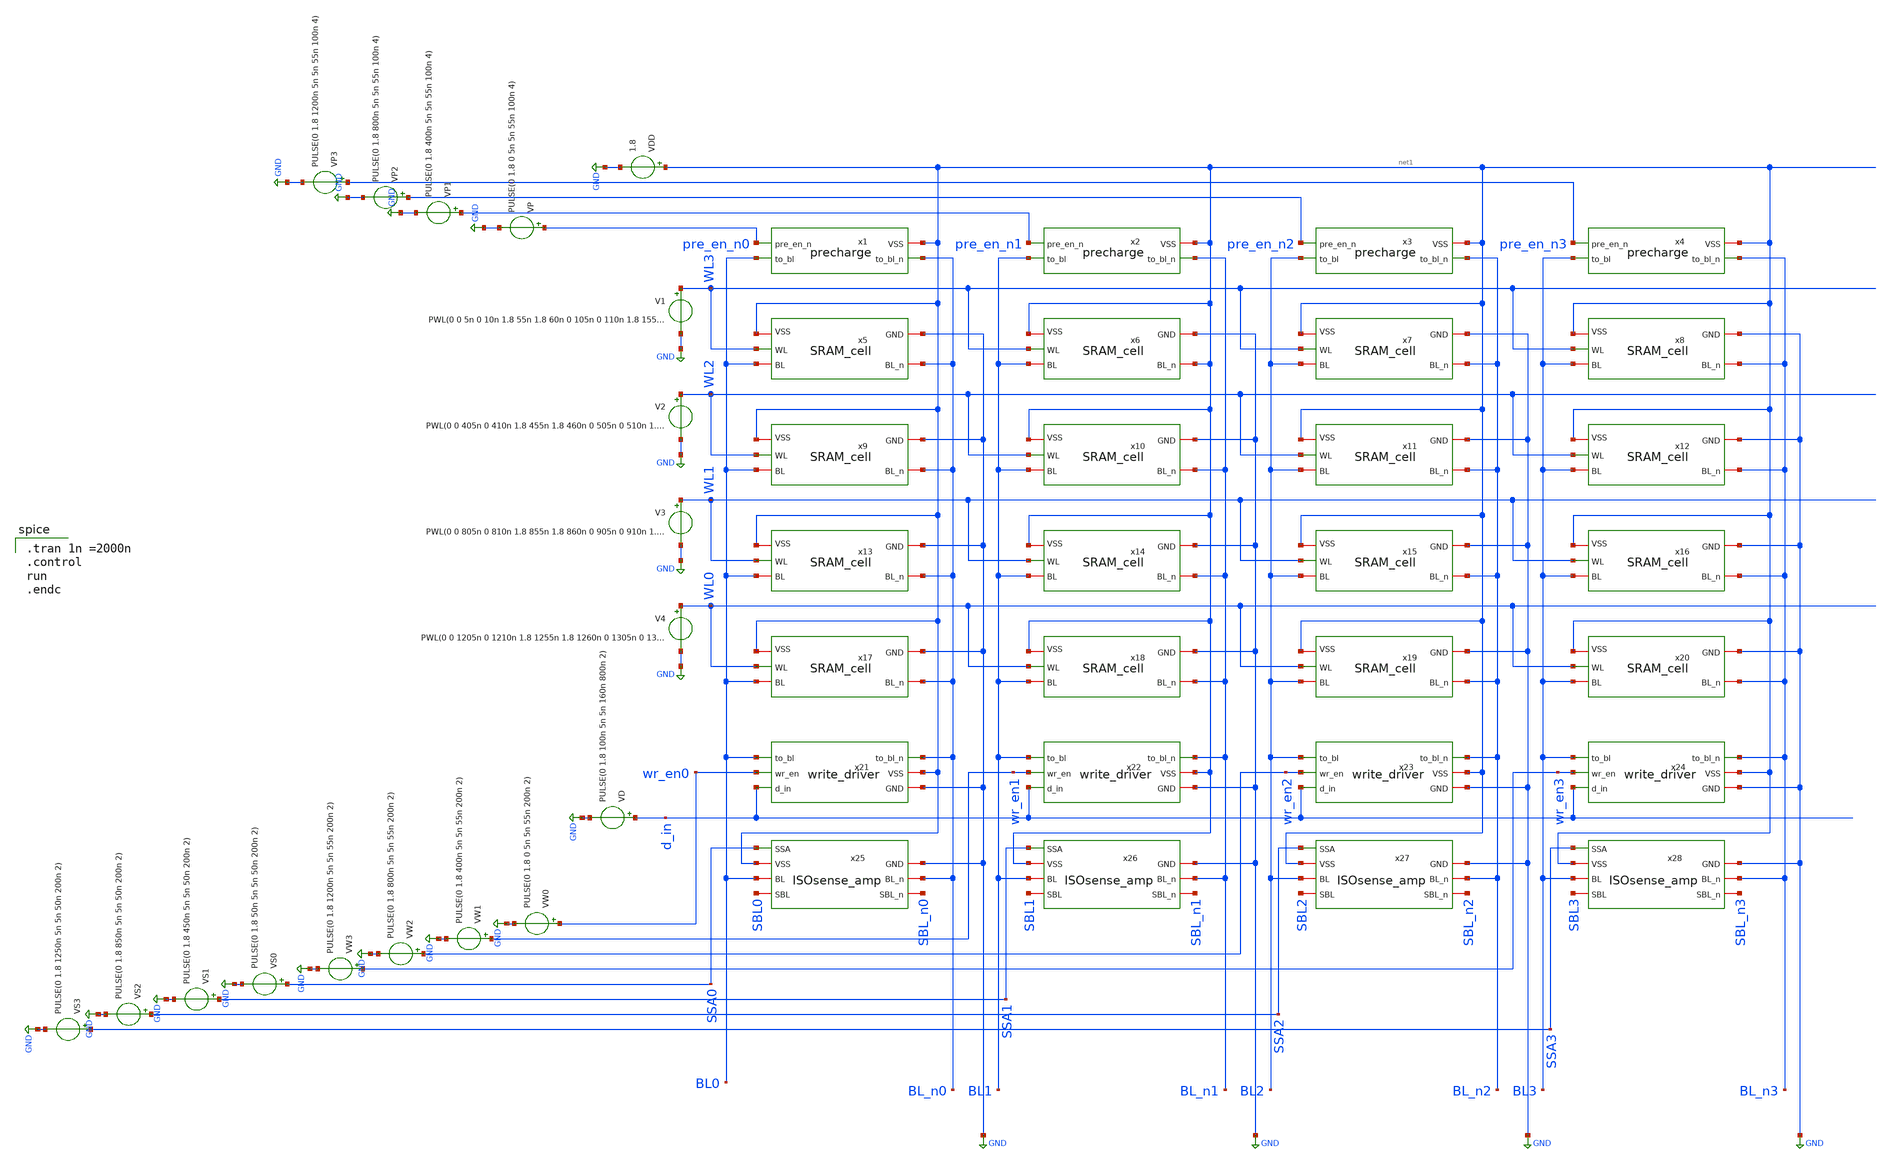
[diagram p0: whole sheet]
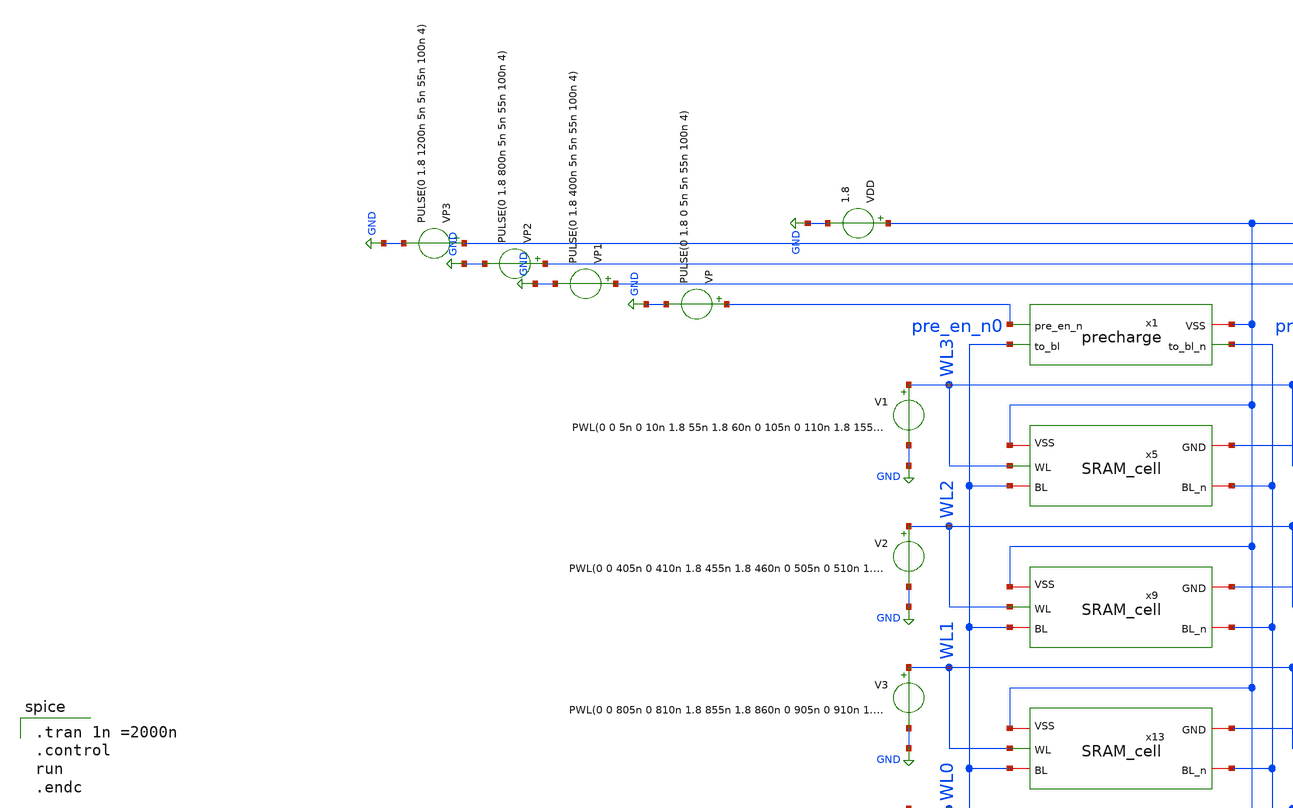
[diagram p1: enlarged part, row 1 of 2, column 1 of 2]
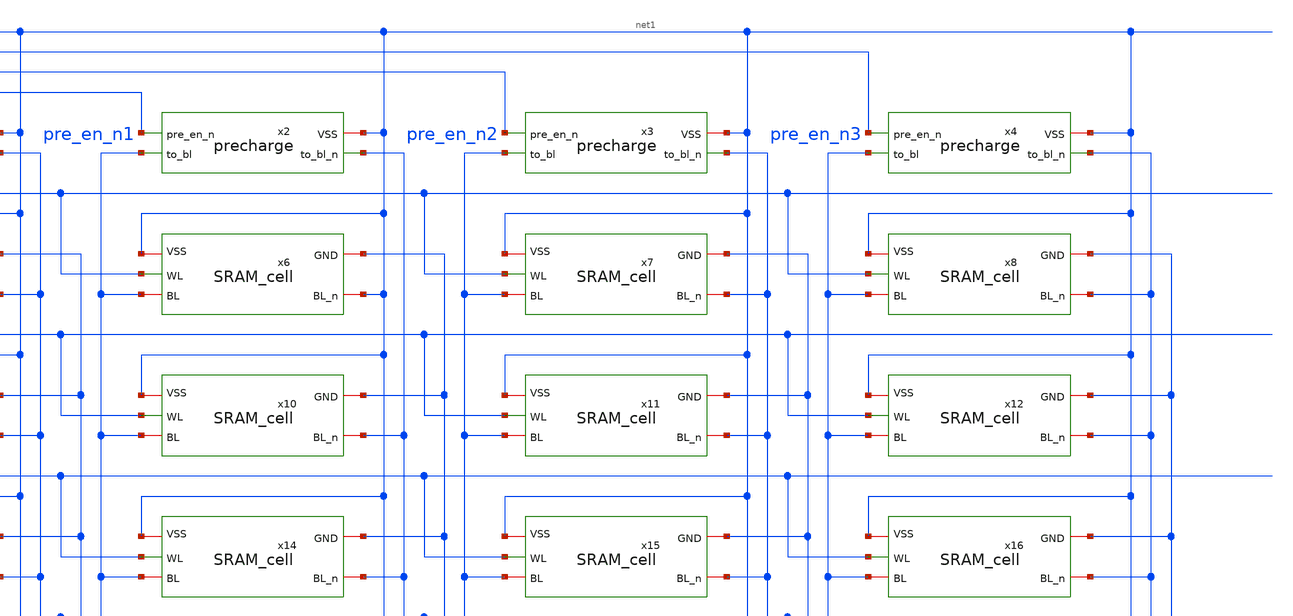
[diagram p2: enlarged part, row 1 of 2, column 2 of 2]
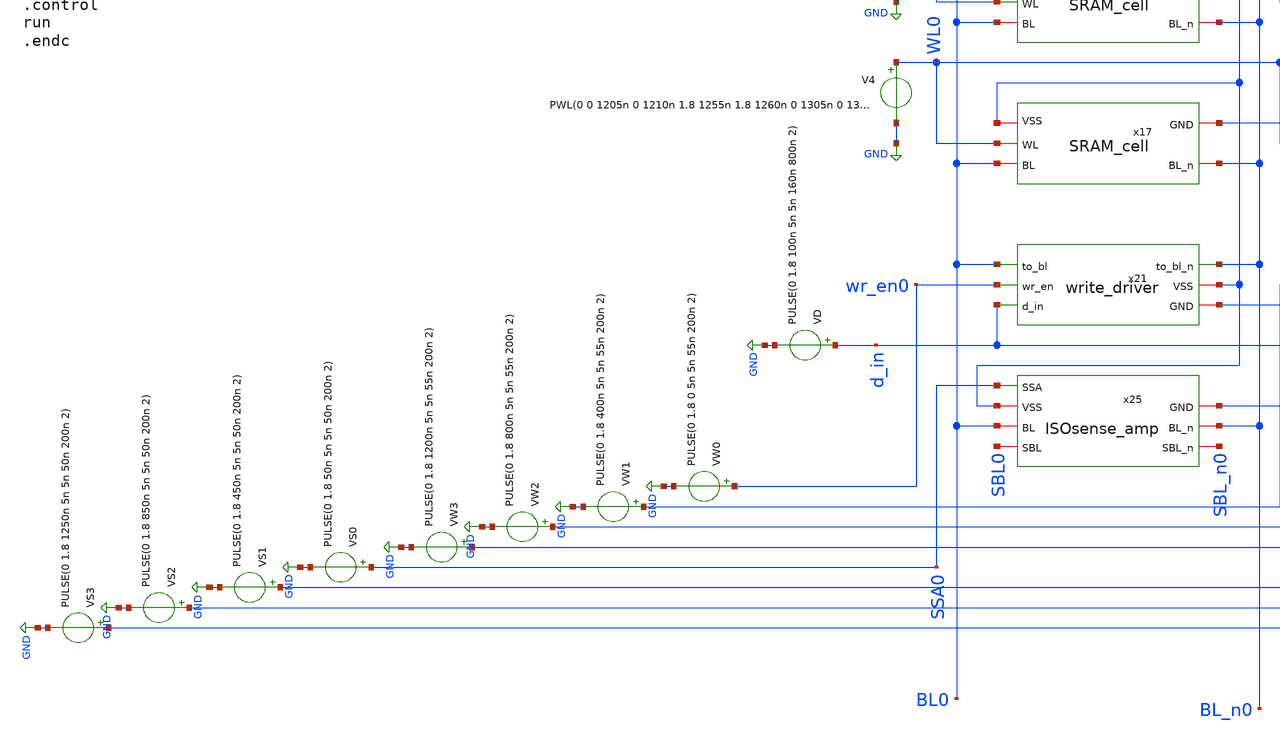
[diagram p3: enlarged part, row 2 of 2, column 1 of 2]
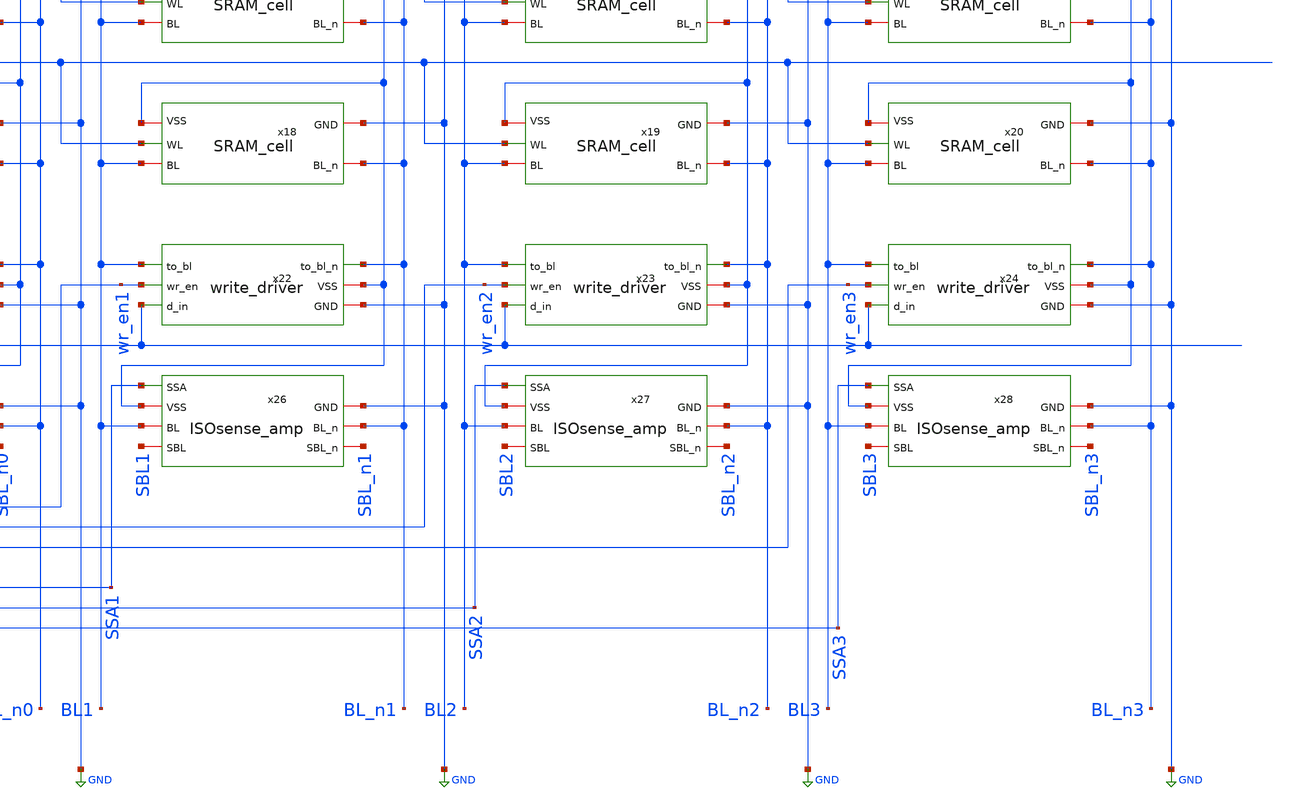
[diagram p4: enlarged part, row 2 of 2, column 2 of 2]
** sch_path: 4x4_SRAM.sch
**.subckt 4x4_SRAM
x1 net1 BL_n0 BL0 pre_en_n0 precharge
x5 WL3 net1 BL_n0 BL0 GND SRAM_cell
x9 WL2 net1 BL_n0 BL0 GND SRAM_cell
x13 WL1 net1 BL_n0 BL0 GND SRAM_cell
x17 WL0 net1 BL_n0 BL0 GND SRAM_cell
x21 BL_n0 BL0 wr_en0 net1 d_in GND write_driver
x25 SSA0 BL0 BL_n0 net1 SBL0 SBL_n0 GND ISOsense_amp
VDD net1 GND 1.8
VP pre_en_n0 GND PULSE(0 1.8 0 5n 5n 55n 100n 4)
V1 WL3 GND PWL(0 0 5n 0 10n 1.8 55n 1.8 60n 0 105n 0 110n 1.8 155n 1.8 160n 0 205n 0 210n 1.8 255n
+ 1.8 260n 0 305n 0 310n 1.8 355n 1.8 360n 0 1600n 0)
VW0 wr_en0 GND PULSE(0 1.8 0 5n 5n 55n 200n 2)
VD d_in GND PULSE(0 1.8 100n 5n 5n 160n 800n 2)
VS0 SSA0 GND PULSE(0 1.8 50n 5n 5n 50n 200n 2)
V2 WL2 GND PWL(0 0 405n 0 410n 1.8 455n 1.8 460n 0 505n 0 510n 1.8 555n 1.8 560n 0 605n 0 610n 1.8
+ 655n 1.8 660n 0 705n 0 710n 1.8 755n 1.8 760n 0 1600n 0)
V3 WL1 GND PWL(0 0 805n 0 810n 1.8 855n 1.8 860n 0 905n 0 910n 1.8 955n 1.8 960n 0 1005n 0 1010n 1.8
+ 1055n 1.8 1060n 0 1105n 0 1110n 1.8 1155n 1.8 1160n 0 1600n 0)
V4 WL0 GND PWL(0 0 1205n 0 1210n 1.8 1255n 1.8 1260n 0 1305n 0 1310n 1.8 1355n 1.8 1360n 0 1405n 0
+ 1410n 1.8 1455n 1.8 1460n 0 1505n 0 1510n 1.8 1555n 1.8 1560n 0 1600n 0
x2 net1 BL_n1 BL1 pre_en_n1 precharge
x3 net1 BL_n2 BL2 pre_en_n2 precharge
x4 net1 BL_n3 BL3 pre_en_n3 precharge
x6 WL3 net1 net1 BL1 GND SRAM_cell
x7 WL3 net1 BL_n2 BL2 GND SRAM_cell
x8 WL3 net1 BL_n3 BL3 GND SRAM_cell
x10 WL2 net1 BL_n1 BL1 GND SRAM_cell
x11 WL2 net1 BL_n2 BL2 GND SRAM_cell
x12 WL2 net1 BL_n3 BL3 GND SRAM_cell
x14 WL1 net1 BL_n1 BL1 GND SRAM_cell
x15 WL1 net1 BL_n2 BL2 GND SRAM_cell
x16 WL1 net1 BL_n3 BL3 GND SRAM_cell
x18 WL0 net1 BL_n1 BL1 GND SRAM_cell
x19 WL0 net1 BL_n2 BL2 GND SRAM_cell
x20 WL0 net1 BL_n3 BL3 GND SRAM_cell
x22 BL_n1 BL1 wr_en1 net1 d_in GND write_driver
x23 BL_n2 BL2 wr_en2 net1 d_in GND write_driver
x24 BL_n3 BL3 wr_en3 net1 d_in GND write_driver
x26 SSA1 BL1 BL_n1 net1 SBL1 SBL_n1 GND ISOsense_amp
x27 SSA2 BL2 BL_n2 net1 SBL2 SBL_n2 GND ISOsense_amp
x28 SSA3 BL3 BL_n3 net1 SBL3 SBL_n3 GND ISOsense_amp
VW1 wr_en1 GND PULSE(0 1.8 400n 5n 5n 55n 200n 2)
VW2 wr_en2 GND PULSE(0 1.8 800n 5n 5n 55n 200n 2)
VW3 wr_en3 GND PULSE(0 1.8 1200n 5n 5n 55n 200n 2)
VS1 SSA1 GND PULSE(0 1.8 450n 5n 5n 50n 200n 2)
VS2 SSA2 GND PULSE(0 1.8 850n 5n 5n 50n 200n 2)
VS3 SSA3 GND PULSE(0 1.8 1250n 5n 5n 50n 200n 2)
VP1 pre_en_n1 GND PULSE(0 1.8 400n 5n 5n 55n 100n 4)
VP2 pre_en_n2 GND PULSE(0 1.8 800n 5n 5n 55n 100n 4)
VP3 pre_en_n3 GND PULSE(0 1.8 1200n 5n 5n 55n 100n 4)
**** begin user architecture code
 .lib $::SKYWATER_MODELS/sky130.lib.spice tt

.tran 1n =2000n
.control
run
.endc

**** end user architecture code
**.ends

* expanding   symbol:  EE431_FINALPROJECT/proj_SRAM/precharge.sym # of pins=4
** sym_path: precharge.sym
** sch_path: precharge.sch
.subckt precharge VSS to_bl_n to_bl pre_en_n
*.ipin pre_en_n
*.opin to_bl
*.opin to_bl_n
*.iopin VSS
XM1 to_bl_n pre_en_n VSS VSS sky130_fd_pr__pfet_01v8 L=0.25 W=0.5 nf=1 ad='int((nf+1)/2) * W/nf * 0.29'
+ as='int((nf+2)/2) * W/nf * 0.29' pd='2*int((nf+1)/2) * (W/nf + 0.29)' ps='2*int((nf+2)/2) * (W/nf + 0.29)'
+ nrd='0.29 / W' nrs='0.29 / W' sa=0 sb=0 sd=0 mult=1 m=1
XM2 to_bl pre_en_n VSS VSS sky130_fd_pr__pfet_01v8 L=0.25 W=0.5 nf=1 ad='int((nf+1)/2) * W/nf * 0.29'
+ as='int((nf+2)/2) * W/nf * 0.29' pd='2*int((nf+1)/2) * (W/nf + 0.29)' ps='2*int((nf+2)/2) * (W/nf + 0.29)'
+ nrd='0.29 / W' nrs='0.29 / W' sa=0 sb=0 sd=0 mult=1 m=1
.ends


* expanding   symbol:  EE431_FINALPROJECT/proj_SRAM/SRAM_cell.sym # of pins=5
** sym_path: SRAM_cell.sym
** sch_path: SRAM_cell.sch
.subckt SRAM_cell WL VSS BL_n BL GND
*.ipin WL
*.iopin BL
*.iopin BL_n
*.iopin VSS
*.iopin GND
XM1 Q_n Q GND GND sky130_fd_pr__nfet_01v8 L=0.25 W=1.25 nf=1 ad='int((nf+1)/2) * W/nf * 0.29' as='int((nf+2)/2) * W/nf * 0.29'
+ pd='2*int((nf+1)/2) * (W/nf + 0.29)' ps='2*int((nf+2)/2) * (W/nf + 0.29)' nrd='0.29 / W' nrs='0.29 / W'
+ sa=0 sb=0 sd=0 mult=1 m=1
XM2 Q_n Q VSS VSS sky130_fd_pr__pfet_01v8 L=0.25 W=0.5 nf=1 ad='int((nf+1)/2) * W/nf * 0.29' as='int((nf+2)/2) * W/nf * 0.29'
+ pd='2*int((nf+1)/2) * (W/nf + 0.29)' ps='2*int((nf+2)/2) * (W/nf + 0.29)' nrd='0.29 / W' nrs='0.29 / W'
+ sa=0 sb=0 sd=0 mult=1 m=1
XM3 Q Q_n GND GND sky130_fd_pr__nfet_01v8 L=0.25 W=1.25 nf=1 ad='int((nf+1)/2) * W/nf * 0.29' as='int((nf+2)/2) * W/nf * 0.29'
+ pd='2*int((nf+1)/2) * (W/nf + 0.29)' ps='2*int((nf+2)/2) * (W/nf + 0.29)' nrd='0.29 / W' nrs='0.29 / W'
+ sa=0 sb=0 sd=0 mult=1 m=1
XM4 Q Q_n VSS VSS sky130_fd_pr__pfet_01v8 L=0.25 W=0.5 nf=1 ad='int((nf+1)/2) * W/nf * 0.29' as='int((nf+2)/2) * W/nf * 0.29'
+ pd='2*int((nf+1)/2) * (W/nf + 0.29)' ps='2*int((nf+2)/2) * (W/nf + 0.29)' nrd='0.29 / W' nrs='0.29 / W'
+ sa=0 sb=0 sd=0 mult=1 m=1
XM5 Q WL BL GND sky130_fd_pr__nfet_01v8 L=0.25 W=0.75 nf=1 ad='int((nf+1)/2) * W/nf * 0.29' as='int((nf+2)/2) * W/nf * 0.29'
+ pd='2*int((nf+1)/2) * (W/nf + 0.29)' ps='2*int((nf+2)/2) * (W/nf + 0.29)' nrd='0.29 / W' nrs='0.29 / W'
+ sa=0 sb=0 sd=0 mult=1 m=1
XM6 Q_n WL BL_n GND sky130_fd_pr__nfet_01v8 L=0.25 W=0.75 nf=1 ad='int((nf+1)/2) * W/nf * 0.29' as='int((nf+2)/2) * W/nf * 0.29'
+ pd='2*int((nf+1)/2) * (W/nf + 0.29)' ps='2*int((nf+2)/2) * (W/nf + 0.29)' nrd='0.29 / W' nrs='0.29 / W'
+ sa=0 sb=0 sd=0 mult=1 m=1
.ends


* expanding   symbol:  EE431_FINALPROJECT/proj_SRAM/write_driver.sym # of pins=6
** sym_path: write_driver.sym
** sch_path: write_driver.sch
.subckt write_driver to_bl_n to_bl wr_en VSS d_in GND
*.ipin d_in
*.ipin wr_en
*.opin to_bl
*.opin to_bl_n
*.iopin VSS
*.iopin GND
XM1 to_bl wr_en d_in GND sky130_fd_pr__nfet_01v8 L=0.25 W=1 nf=1 ad='int((nf+1)/2) * W/nf * 0.29' as='int((nf+2)/2) * W/nf * 0.29'
+ pd='2*int((nf+1)/2) * (W/nf + 0.29)' ps='2*int((nf+2)/2) * (W/nf + 0.29)' nrd='0.29 / W' nrs='0.29 / W'
+ sa=0 sb=0 sd=0 mult=1 m=1
XM2 to_bl_n wr_en d_n GND sky130_fd_pr__nfet_01v8 L=0.25 W=1 nf=1 ad='int((nf+1)/2) * W/nf * 0.29' as='int((nf+2)/2) * W/nf * 0.29'
+ pd='2*int((nf+1)/2) * (W/nf + 0.29)' ps='2*int((nf+2)/2) * (W/nf + 0.29)' nrd='0.29 / W' nrs='0.29 / W'
+ sa=0 sb=0 sd=0 mult=1 m=1
XM3 d_n d_in VSS VSS sky130_fd_pr__pfet_01v8 L=0.25 W=1 nf=1 ad='int((nf+1)/2) * W/nf * 0.29' as='int((nf+2)/2) * W/nf * 0.29'
+ pd='2*int((nf+1)/2) * (W/nf + 0.29)' ps='2*int((nf+2)/2) * (W/nf + 0.29)' nrd='0.29 / W' nrs='0.29 / W'
+ sa=0 sb=0 sd=0 mult=1 m=1
XM4 d_n d_in GND GND sky130_fd_pr__nfet_01v8 L=0.25 W=0.5 nf=1 ad='int((nf+1)/2) * W/nf * 0.29' as='int((nf+2)/2) * W/nf * 0.29'
+ pd='2*int((nf+1)/2) * (W/nf + 0.29)' ps='2*int((nf+2)/2) * (W/nf + 0.29)' nrd='0.29 / W' nrs='0.29 / W'
+ sa=0 sb=0 sd=0 mult=1 m=1
.ends


* expanding   symbol:  EE431_FINALPROJECT/proj_SRAM/ISOsense_amp.sym # of pins=7
** sym_path: ISOsense_amp.sym
** sch_path: ISOsense_amp.sch
.subckt ISOsense_amp SSA BL BL_n VSS SBL SBL_n GND
*.iopin VSS
*.iopin BL_n
*.iopin BL
*.iopin GND
*.ipin SSA
*.iopin SBL
*.iopin SBL_n
XM1 SBL_n SBL net1 GND sky130_fd_pr__nfet_01v8 L=0.25 W=1 nf=1 ad='int((nf+1)/2) * W/nf * 0.29' as='int((nf+2)/2) * W/nf * 0.29'
+ pd='2*int((nf+1)/2) * (W/nf + 0.29)' ps='2*int((nf+2)/2) * (W/nf + 0.29)' nrd='0.29 / W' nrs='0.29 / W'
+ sa=0 sb=0 sd=0 mult=1 m=1
XM2 SBL SBL_n net1 GND sky130_fd_pr__nfet_01v8 L=0.25 W=1 nf=1 ad='int((nf+1)/2) * W/nf * 0.29' as='int((nf+2)/2) * W/nf * 0.29'
+ pd='2*int((nf+1)/2) * (W/nf + 0.29)' ps='2*int((nf+2)/2) * (W/nf + 0.29)' nrd='0.29 / W' nrs='0.29 / W'
+ sa=0 sb=0 sd=0 mult=1 m=1
XM3 SBL_n SBL VSS VSS sky130_fd_pr__pfet_01v8 L=0.25 W=2 nf=1 ad='int((nf+1)/2) * W/nf * 0.29' as='int((nf+2)/2) * W/nf * 0.29'
+ pd='2*int((nf+1)/2) * (W/nf + 0.29)' ps='2*int((nf+2)/2) * (W/nf + 0.29)' nrd='0.29 / W' nrs='0.29 / W'
+ sa=0 sb=0 sd=0 mult=1 m=1
XM4 SBL SBL_n VSS VSS sky130_fd_pr__pfet_01v8 L=0.25 W=2 nf=1 ad='int((nf+1)/2) * W/nf * 0.29' as='int((nf+2)/2) * W/nf * 0.29'
+ pd='2*int((nf+1)/2) * (W/nf + 0.29)' ps='2*int((nf+2)/2) * (W/nf + 0.29)' nrd='0.29 / W' nrs='0.29 / W'
+ sa=0 sb=0 sd=0 mult=1 m=1
XM5 net1 SSA GND GND sky130_fd_pr__nfet_01v8 L=0.25 W=2 nf=1 ad='int((nf+1)/2) * W/nf * 0.29' as='int((nf+2)/2) * W/nf * 0.29'
+ pd='2*int((nf+1)/2) * (W/nf + 0.29)' ps='2*int((nf+2)/2) * (W/nf + 0.29)' nrd='0.29 / W' nrs='0.29 / W'
+ sa=0 sb=0 sd=0 mult=1 m=1
XM6 SBL SSA BL VSS sky130_fd_pr__pfet_01v8 L=0.25 W=0.5 nf=1 ad='int((nf+1)/2) * W/nf * 0.29' as='int((nf+2)/2) * W/nf * 0.29'
+ pd='2*int((nf+1)/2) * (W/nf + 0.29)' ps='2*int((nf+2)/2) * (W/nf + 0.29)' nrd='0.29 / W' nrs='0.29 / W'
+ sa=0 sb=0 sd=0 mult=1 m=1
XM7 SBL_n SSA BL_n VSS sky130_fd_pr__pfet_01v8 L=0.25 W=0.5 nf=1 ad='int((nf+1)/2) * W/nf * 0.29' as='int((nf+2)/2) * W/nf * 0.29'
+ pd='2*int((nf+1)/2) * (W/nf + 0.29)' ps='2*int((nf+2)/2) * (W/nf + 0.29)' nrd='0.29 / W' nrs='0.29 / W'
+ sa=0 sb=0 sd=0 mult=1 m=1
.ends

.GLOBAL GND
.end
